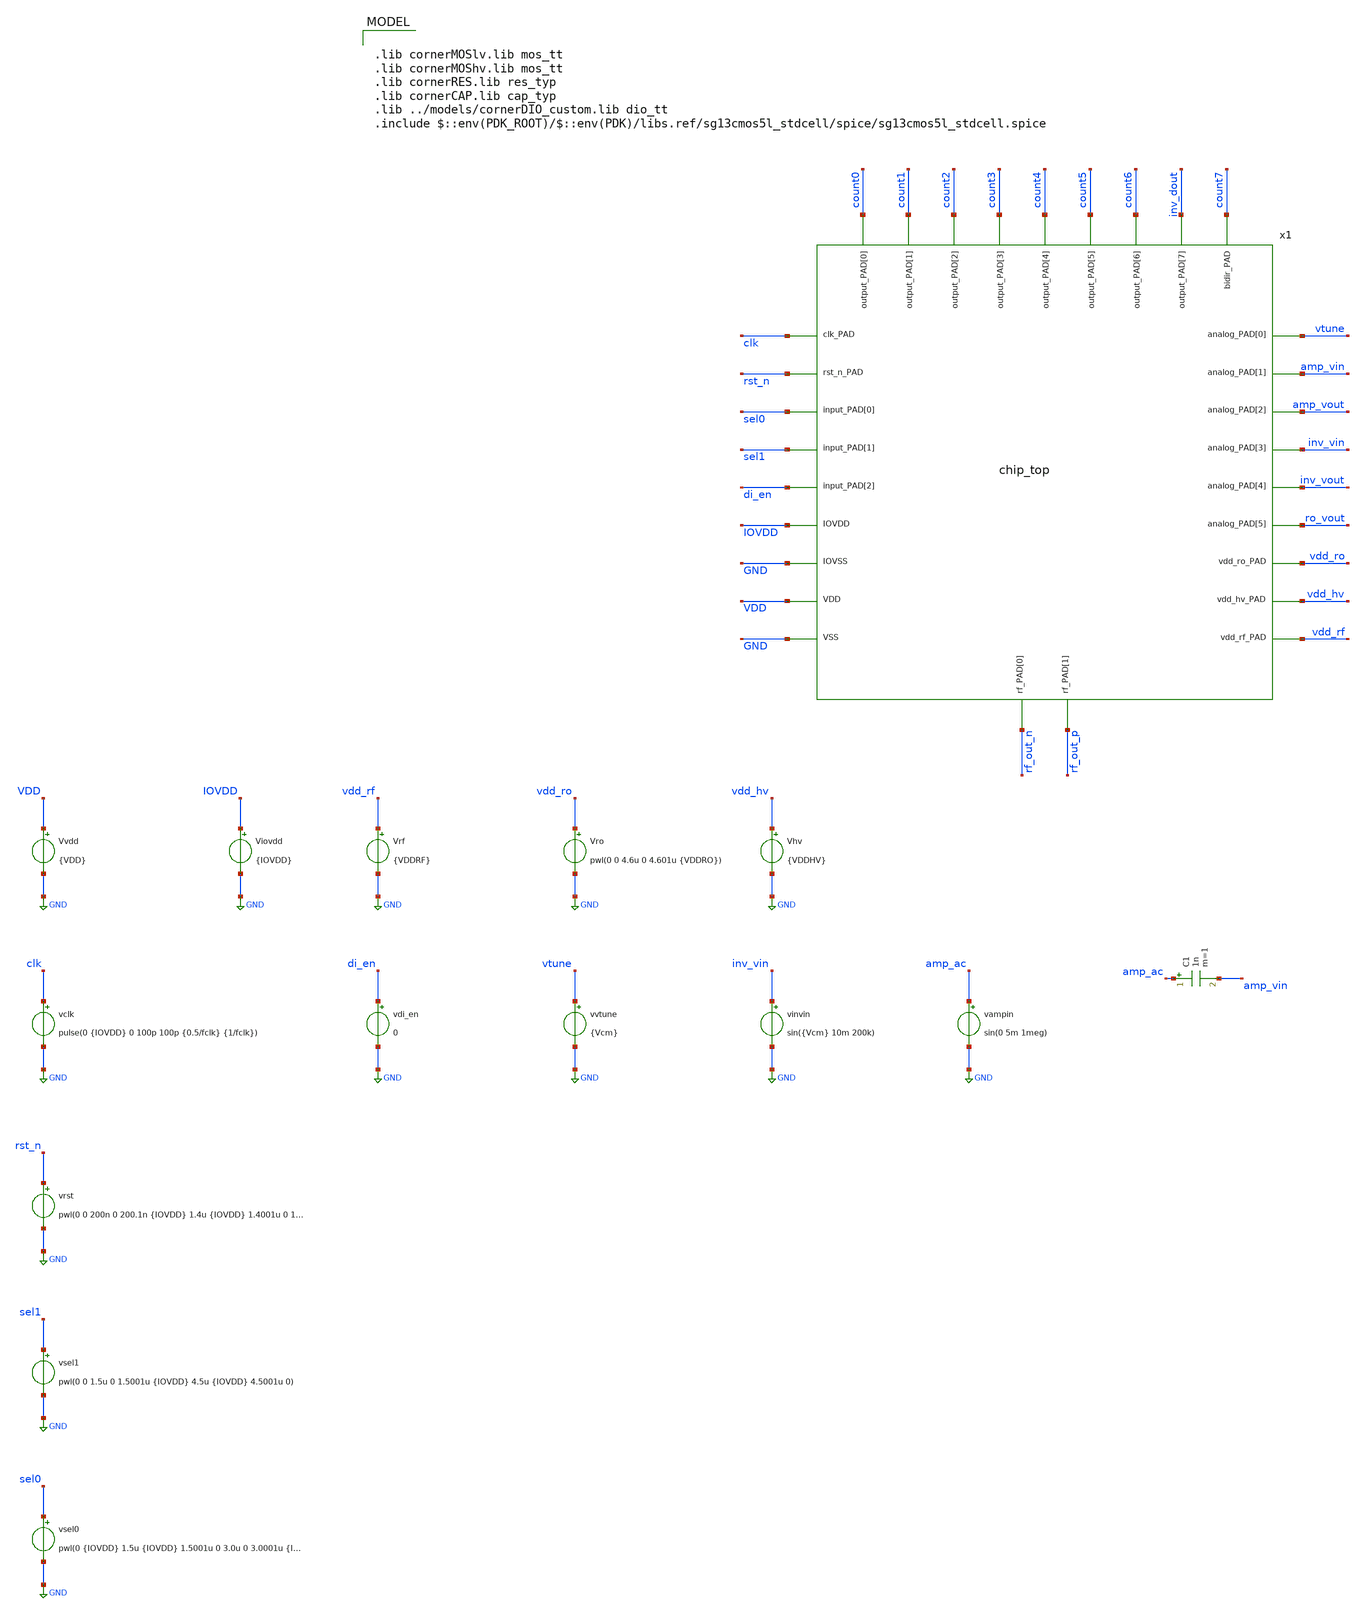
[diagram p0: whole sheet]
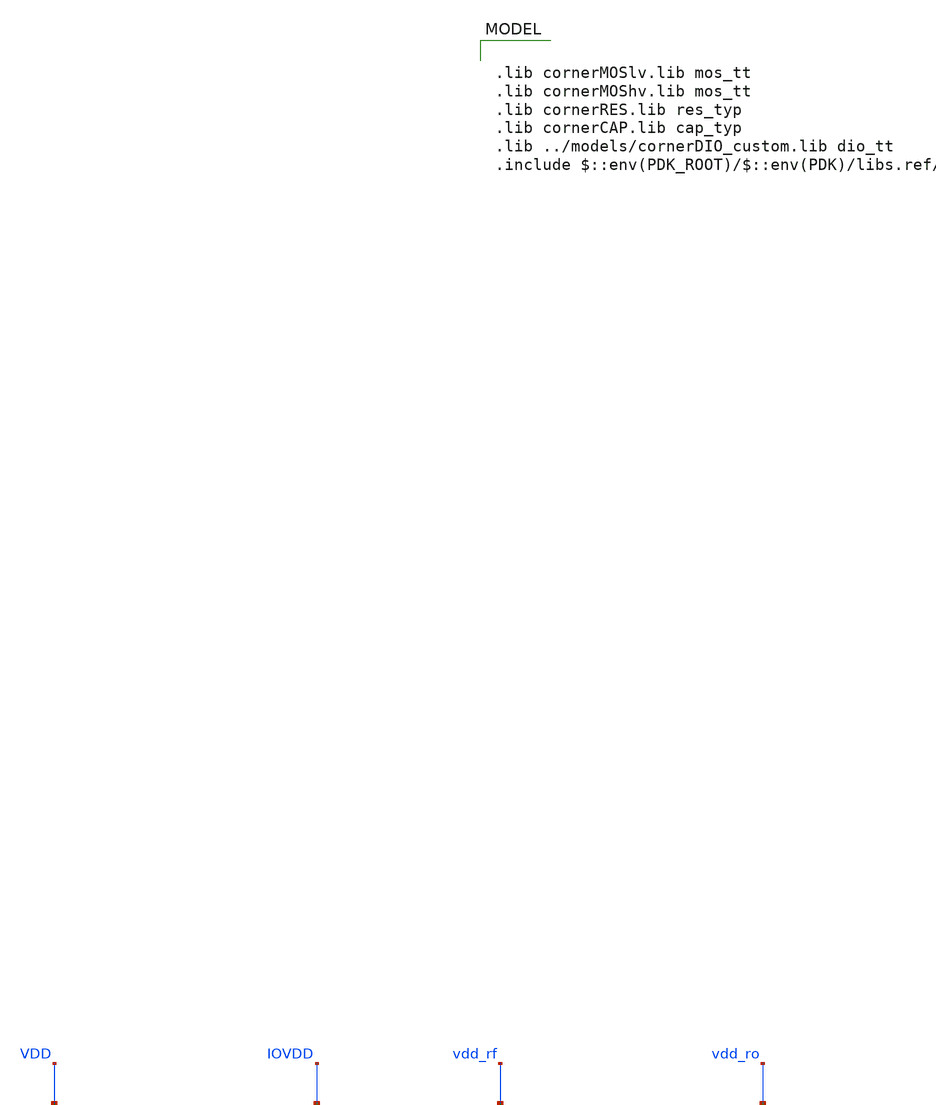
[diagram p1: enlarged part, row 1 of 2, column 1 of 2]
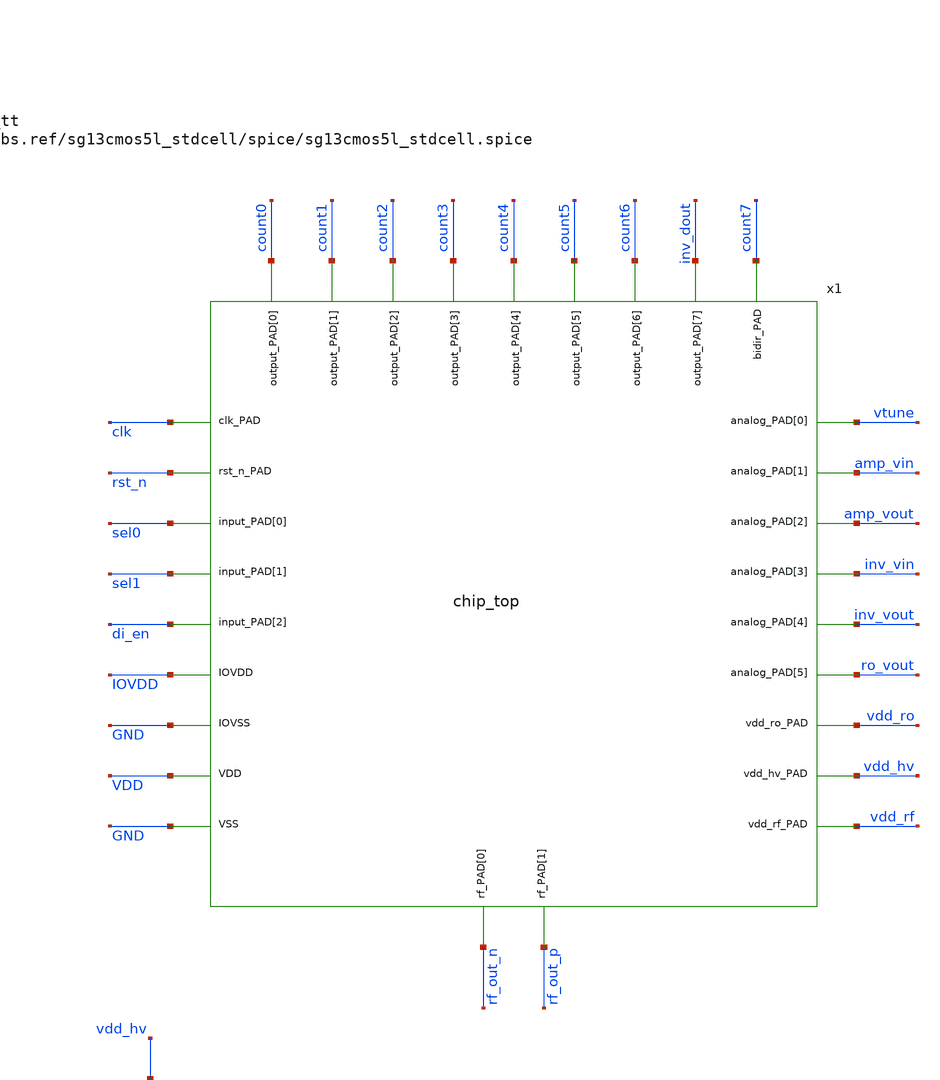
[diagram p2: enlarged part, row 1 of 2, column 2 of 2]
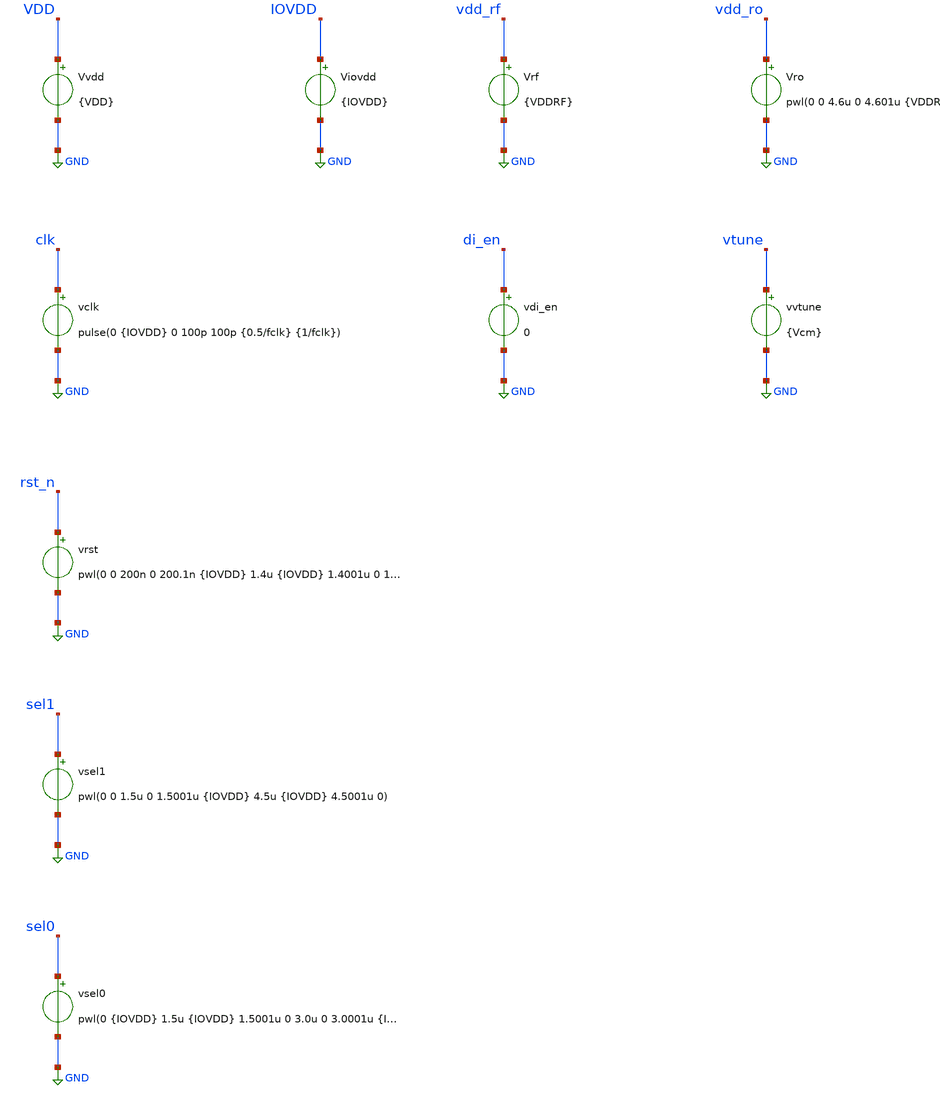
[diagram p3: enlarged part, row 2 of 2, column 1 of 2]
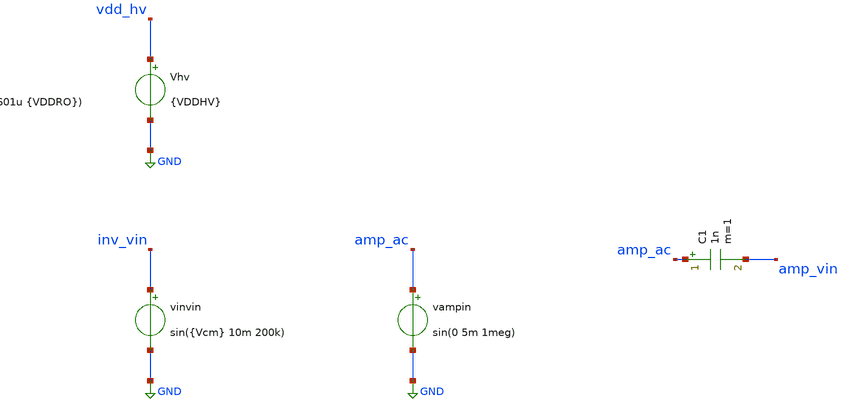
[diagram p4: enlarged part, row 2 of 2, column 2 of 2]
** sch_path: testbenches/xschem/chip_top_tb_tran.sch
**.subckt chip_top_tb_tran
x1 clk rst_n sel0 sel1 di_en IOVDD GND VDD GND vtune amp_vin amp_vout inv_vin inv_vout ro_vout
+ vdd_ro vdd_hv vdd_rf count0 count1 count2 count3 count4 count5 count6 inv_dout count7 rf_out_n rf_out_p
+ chip_top
Vvdd VDD GND {VDD}
Viovdd IOVDD GND {IOVDD}
Vrf vdd_rf GND {VDDRF}
Vro vdd_ro GND pwl(0 0 4.6u 0 4.601u {VDDRO})
Vhv vdd_hv GND {VDDHV}
vclk clk GND pulse(0 {IOVDD} 0 100p 100p {0.5/fclk} {1/fclk})
vrst rst_n GND pwl(0 0 200n 0 200.1n {IOVDD} 1.4u {IOVDD} 1.4001u 0 1.7u 0 1.7001u {IOVDD} 2.9u {IOVDD}
+ 2.9001u 0 3.2u 0 3.2001u {IOVDD} 4.4u {IOVDD} 4.4001u 0 4.7u 0 4.7001u {IOVDD})
vsel1 sel1 GND pwl(0 0 1.5u 0 1.5001u {IOVDD} 4.5u {IOVDD} 4.5001u 0)
vsel0 sel0 GND pwl(0 {IOVDD} 1.5u {IOVDD} 1.5001u 0 3.0u 0 3.0001u {IOVDD} 4.5u {IOVDD} 4.5001u 0)
vdi_en di_en GND 0
vvtune vtune GND {Vcm}
vinvin inv_vin GND sin({Vcm} 10m 200k)
vampin amp_ac GND sin(0 5m 1meg)
C1 amp_ac amp_vin 1n m=1
**** begin user architecture code


.include ../../../ip/sg13cmos5l_io_custom/spice/sg13cmos5l_io.spi
.include ../../../macros/counter_lv_ihp/netlist/xspice/counter_lv_ihp_top.xspice
* The XSPICE model of the HV counter is built for 3.3 V, and the one of the ETH counter keeps the
*+ unknown states that slow edges feed into it,
* so the bench uses the post-layout netlists of these two
.include ../../../macros/counter_lv_eth/netlist/pex/counter_lv_eth_top_magic_pex_3.spice
.include ../../../macros/counter_hv_kvc/netlist/pex/counter_hv_kvc_top_magic_pex_3.spice
.include ../../../macros/vco/netlist/spice/vco_ind_le.spice
.param IOVDD=3.3
.param VDD=1.2
.param VDDRF=1.5
.param VDDRO=1.2
.param VDDHV=1.2
.param Vcm=0.6
.temp 27
.param fclk=50e6
.csparam fclk=fclk
.param Cload=10p
.param Rload=1k
* The ring oscillator sets the time step, so it only starts 400 ns before the end of the run
* Package and instrument loads
Cl0 count0 0 {Cload}
Cl1 count1 0 {Cload}
Cl2 count2 0 {Cload}
Cl3 count3 0 {Cload}
Cl4 count4 0 {Cload}
Cl5 count5 0 {Cload}
Cl6 count6 0 {Cload}
Cl7 count7 0 {Cload}
Cl8 inv_dout 0 {Cload}
Cl9 ro_vout 0 1p
Rl1 amp_vout 0 {Rload*100}
Cl10 amp_vout 0 1p
Rl2 inv_vout 0 {Rload*100}
Cl11 inv_vout 0 1p
Rrfn rf_out_n 0 50
Rrfp rf_out_p 0 50
.options klu method=gear reltol=3e-3 vntol=1e-5 abstol=1e-11 chgtol=1e-11 rshunt=1e15
.control

set num_threads=16

save clk rst_n sel1 sel0 di_en count0 count1 count2 count3 count4 count5 count6 count7 inv_dout
+ inv_vin inv_vout amp_vin amp_vout ro_vout rf_out_n rf_out_p i(Vvdd) i(Vhv) i(Vro) i(Vrf) i(Viovdd)

* User Constants
let tstart = 0
let tstop = 5u
let tstep = 100p

* Transient Operating Point Analysis
op
remzerovec
write @schname\.raw
set appendwrite

* Transient Analysis
tran $&tstep $&tstop $&tstart
write @schname\.raw

* Write Data
unset appendwrite
set wr_vecnames
set wr_singlescale
wrdata ../plot_simulations/data/chip_top_tb_tran.txt  v(clk) v(rst_n) v(sel1) v(sel0) v(di_en)
+  v(count0) v(count1) v(count2) v(count3) v(count4) v(count5) v(count6) v(count7)  v(inv_dout) v(inv_vin)
+ v(inv_vout) v(amp_vin) v(amp_vout) v(ro_vout)  i(Vvdd) i(Vhv) i(Vro)
.endc



.lib cornerMOSlv.lib mos_tt
.lib cornerMOShv.lib mos_tt
.lib cornerRES.lib res_typ
.lib cornerCAP.lib cap_typ
.lib ../models/cornerDIO_custom.lib dio_tt
.include $::env(PDK_ROOT)/$::env(PDK)/libs.ref/sg13cmos5l_stdcell/spice/sg13cmos5l_stdcell.spice

**** end user architecture code
**.ends
.GLOBAL GND
.end
